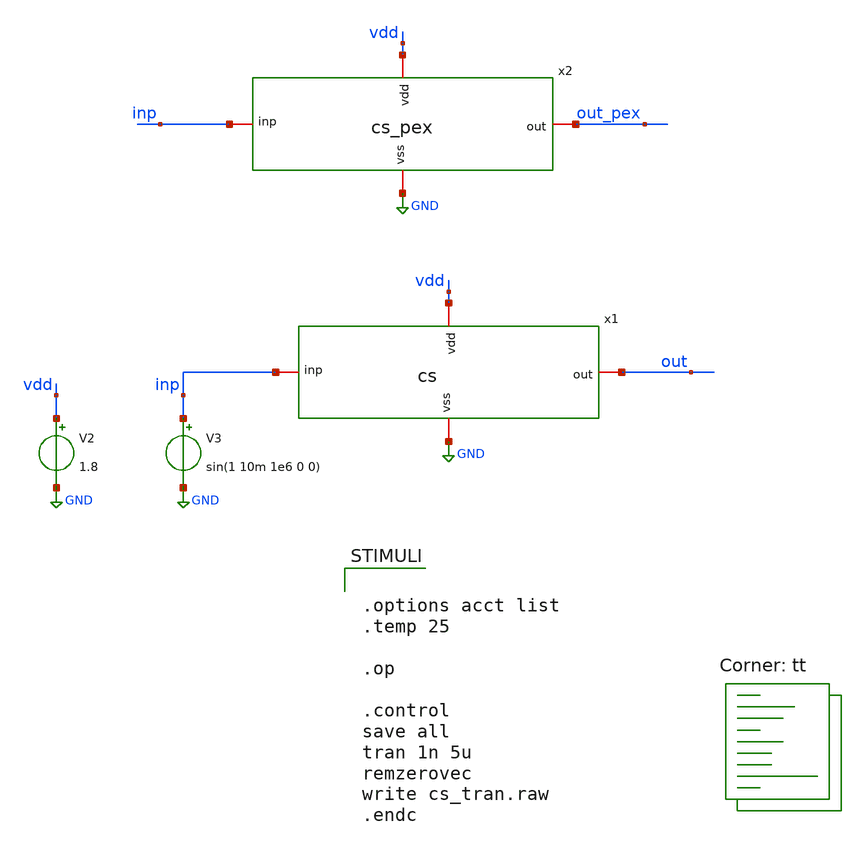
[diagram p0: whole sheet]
** sch_path: xschem/cs/cs_tran.sch
**.subckt cs_tran
x1 vdd out inp GND cs
V2 vdd GND 1.8
V3 inp GND sin(1 10m 1e6 0 0)
x2 vdd out_pex inp GND cs_pex
**** begin user architecture code
.lib $::SKYWATER_MODELS/sky130.lib.spice tt


.options acct list
.temp 25

.op

.control
save all
tran 1n 5u
remzerovec
write cs_tran.raw
.endc


**** end user architecture code
**.ends

* expanding   symbol:  cs/cs.sym # of pins=4
** sym_path: xschem/cs/cs.sym
** sch_path: xschem/cs/cs.sch
.subckt cs vdd out inp vss
*.iopin inp
*.iopin out
*.iopin vdd
*.iopin vss
XM1 out inp vss vss sky130_fd_pr__nfet_01v8 L=0.15 W=50 nf=1 ad='int((nf+1)/2) * W/nf * 0.29' as='int((nf+2)/2) * W/nf * 0.29'
+ pd='2*int((nf+1)/2) * (W/nf + 0.29)' ps='2*int((nf+2)/2) * (W/nf + 0.29)' nrd='0.29 / W' nrs='0.29 / W'
+ sa=0 sb=0 sd=0 mult=1 m=1
XR1 out vdd vss sky130_fd_pr__res_high_po_1p41 L=0.5 mult=1 m=1
.ends


* expanding   symbol:  cs/cs_pex.sym # of pins=4
** sym_path: xschem/cs/cs.sym
.include /home/vks/pll/magic/cs_pex.spice
.GLOBAL GND
.end
